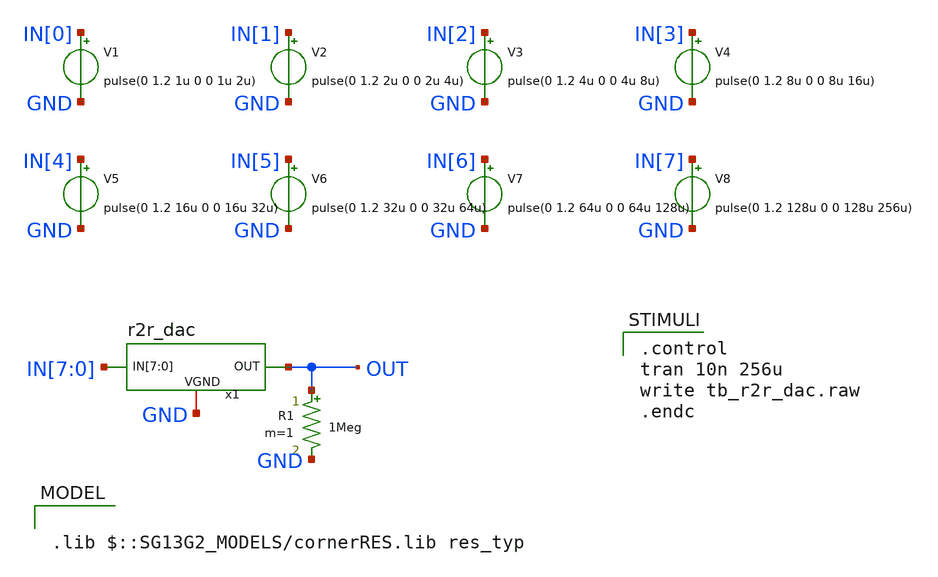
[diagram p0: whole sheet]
** sch_path: xschem/tb_r2r_dac.sch
**.subckt tb_r2r_dac
x1 IN[7] IN[6] IN[5] IN[4] IN[3] IN[2] IN[1] IN[0] OUT GND r2r_dac
V4 IN[3] GND pulse(0 1.2 8u 0 0 8u 16u)
V3 IN[2] GND pulse(0 1.2 4u 0 0 4u 8u)
V2 IN[1] GND pulse(0 1.2 2u 0 0 2u 4u)
V1 IN[0] GND pulse(0 1.2 1u 0 0 1u 2u)
R1 OUT GND 1Meg m=1
V8 IN[7] GND pulse(0 1.2 128u 0 0 128u 256u)
V7 IN[6] GND pulse(0 1.2 64u 0 0 64u 128u)
V6 IN[5] GND pulse(0 1.2 32u 0 0 32u 64u)
V5 IN[4] GND pulse(0 1.2 16u 0 0 16u 32u)
**** begin user architecture code

.control
tran 10n 256u
write tb_r2r_dac.raw
.endc


.lib $::SG13G2_MODELS/cornerRES.lib res_typ

**** end user architecture code
**.ends

* expanding   symbol:  r2r_dac.sym # of pins=3
** sym_path: xschem/r2r_dac.sym
** sch_path: xschem/r2r_dac.sch
.subckt r2r_dac IN[7] IN[6] IN[5] IN[4] IN[3] IN[2] IN[1] IN[0] OUT VGND
*.ipin IN[7],IN[6],IN[5],IN[4],IN[3],IN[2],IN[1],IN[0]
*.iopin VGND
*.opin OUT
XR0a IN[0] wi0 VGND rhigh w=2u l=14.3u m=1 b=0 mm_ok=1
XR0b wi0 wJ0 VGND rhigh w=2u l=14.3u m=1 b=0 mm_ok=1
XR1c wJ1 wJ0 VGND rhigh w=2u l=14.3u m=1 b=0 mm_ok=1
XR0c wJ0 wg0 VGND rhigh w=2u l=14.3u m=1 b=0 mm_ok=1
XR0d wg0 VGND VGND rhigh w=2u l=14.3u m=1 b=0 mm_ok=1
XR1a IN[1] wi1 VGND rhigh w=2u l=14.3u m=1 b=0 mm_ok=1
XR1b wi1 wJ1 VGND rhigh w=2u l=14.3u m=1 b=0 mm_ok=1
XR2c wJ2 wJ1 VGND rhigh w=2u l=14.3u m=1 b=0 mm_ok=1
XR2a IN[2] wi2 VGND rhigh w=2u l=14.3u m=1 b=0 mm_ok=1
XR2b wi2 wJ2 VGND rhigh w=2u l=14.3u m=1 b=0 mm_ok=1
XR3c wJ3 wJ2 VGND rhigh w=2u l=14.3u m=1 b=0 mm_ok=1
XR3a IN[3] wi3 VGND rhigh w=2u l=14.3u m=1 b=0 mm_ok=1
XR3b wi3 wJ3 VGND rhigh w=2u l=14.3u m=1 b=0 mm_ok=1
XR4c wJ4 wJ3 VGND rhigh w=2u l=14.3u m=1 b=0 mm_ok=1
XR4a IN[4] wi4 VGND rhigh w=2u l=14.3u m=1 b=0 mm_ok=1
XR4b wi4 wJ4 VGND rhigh w=2u l=14.3u m=1 b=0 mm_ok=1
XR5c wJ5 wJ4 VGND rhigh w=2u l=14.3u m=1 b=0 mm_ok=1
XR5a IN[5] wi5 VGND rhigh w=2u l=14.3u m=1 b=0 mm_ok=1
XR5b wi5 wJ5 VGND rhigh w=2u l=14.3u m=1 b=0 mm_ok=1
XR6c wJ6 wJ5 VGND rhigh w=2u l=14.3u m=1 b=0 mm_ok=1
XR6a IN[6] wi6 VGND rhigh w=2u l=14.3u m=1 b=0 mm_ok=1
XR6b wi6 wJ6 VGND rhigh w=2u l=14.3u m=1 b=0 mm_ok=1
XR7c OUT wJ6 VGND rhigh w=2u l=14.3u m=1 b=0 mm_ok=1
XR7a IN[7] wi7 VGND rhigh w=2u l=14.3u m=1 b=0 mm_ok=1
XR7b wi7 OUT VGND rhigh w=2u l=14.3u m=1 b=0 mm_ok=1
XRdummy1 VGND VGND VGND rhigh w=2u l=14.3u m=1 b=0 mm_ok=1
XRdummy2 VGND VGND VGND rhigh w=2u l=14.3u m=1 b=0 mm_ok=1
.ends

.end
